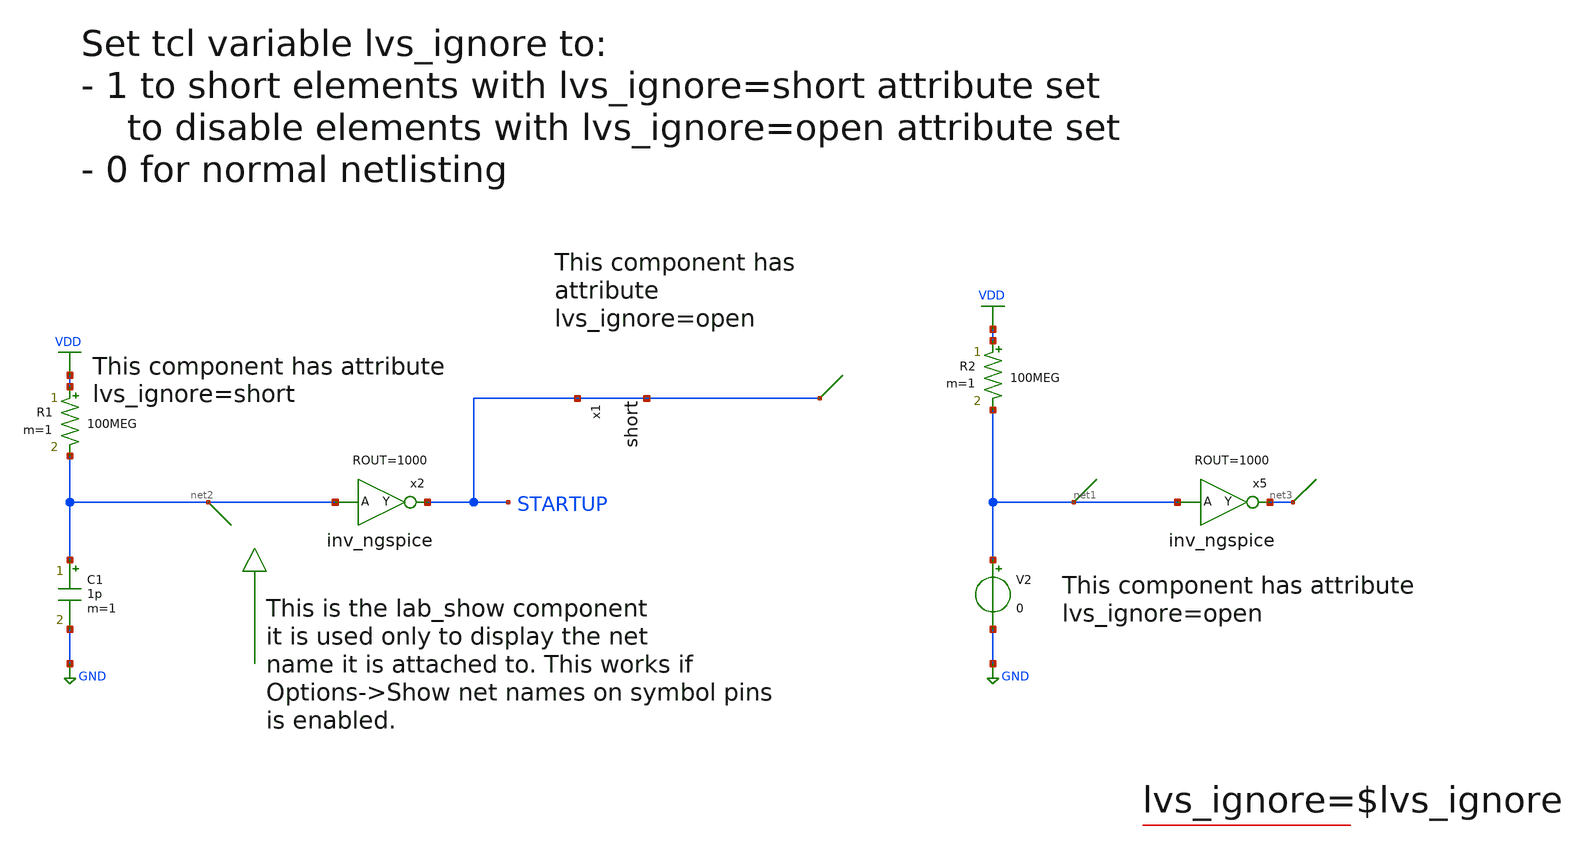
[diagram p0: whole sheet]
** sch_path: xschem_libs_newsym/examples/test_lvs_ignore/schematic/test_lvs_ignore.sch
* Copyright (C) 1998-2024 Stefan Frederik Schippers
* This program is free software; you can redistribute it and/or modify
* it under the terms of the GNU General Public License as published by
* the Free Software Foundation; either version 2 of the License, or
* (at your option) any later version.
* This program is distributed in the hope that it will be useful,
* but WITHOUT ANY WARRANTY; without even the implied warranty of
* MERCHANTABILITY or FITNESS FOR A PARTICULAR PURPOSE.  See the
* GNU General Public License for more details.
* You should have received a copy of the GNU General Public License
* along with this program; if not, write to the Free Software
**.subckt test_lvs_ignore
V2 net1 GND 0
x5 net3 net1 inv_ngspice ROUT=1000
R1 VDD net2 100MEG m=1
C1 net2 GND 1p m=1
x2 STARTUP net2 inv_ngspice ROUT=1000
R2 VDD net1 100MEG m=1
* short x1 : STARTUP <--> STARTUP
**.ends

* expanding   symbol:  ngspice/inv_ngspice.sym # of pins=2
** sym_path: ngspice/inv_ngspice.sym
** sch_path: ngspice/inv_ngspice.sch
.subckt inv_ngspice Y A  ROUT=1000
*.ipin A
*.opin Y
B1 net1 0 V = 'VCC/2*(1-tanh((V(A1)-VCC/2)*100))'
R1 Y1 net1 'ROUT' m=1
C1 A1 0 8f m=1
C2 Y1 0 8f m=1
V1 Y Y1 0
V2 A1 A 0
.ends

.GLOBAL GND
.GLOBAL VDD
.end
